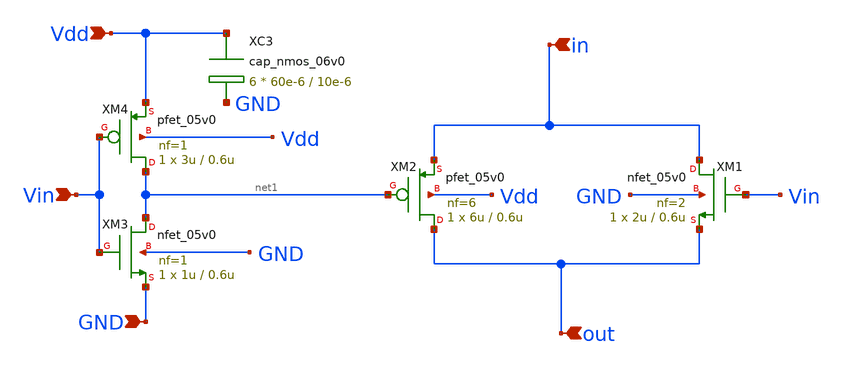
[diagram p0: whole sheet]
** sch_path: schema_ram/MG_switch/cmos_switch.sch
**.subckt cmos_switch Vdd Vin in out GND
*.ipin Vdd
*.ipin Vin
*.ipin in
*.ipin out
*.ipin GND
XM1 in Vin out GND nfet_05v0 L=0.6u W=2u nf=2 ad='int((nf+1)/2) * W/nf * 0.18u' as='int((nf+2)/2) * W/nf * 0.18u'
+ pd='2*int((nf+1)/2) * (W/nf + 0.18u)' ps='2*int((nf+2)/2) * (W/nf + 0.18u)' nrd='0.18u / W' nrs='0.18u / W'
+ sa=0 sb=0 sd=0 m=1
XM2 out net1 in Vdd pfet_05v0 L=0.6u W=6u nf=6 ad='int((nf+1)/2) * W/nf * 0.18u' as='int((nf+2)/2) * W/nf * 0.18u'
+ pd='2*int((nf+1)/2) * (W/nf + 0.18u)' ps='2*int((nf+2)/2) * (W/nf + 0.18u)' nrd='0.18u / W' nrs='0.18u / W'
+ sa=0 sb=0 sd=0 m=1
XM3 net1 Vin GND GND nfet_05v0 L=0.6u W=1u nf=1 ad='int((nf+1)/2) * W/nf * 0.18u' as='int((nf+2)/2) * W/nf * 0.18u'
+ pd='2*int((nf+1)/2) * (W/nf + 0.18u)' ps='2*int((nf+2)/2) * (W/nf + 0.18u)' nrd='0.18u / W' nrs='0.18u / W'
+ sa=0 sb=0 sd=0 m=1
XM4 net1 Vin Vdd Vdd pfet_05v0 L=0.6u W=3u nf=1 ad='int((nf+1)/2) * W/nf * 0.18u' as='int((nf+2)/2) * W/nf * 0.18u'
+ pd='2*int((nf+1)/2) * (W/nf + 0.18u)' ps='2*int((nf+2)/2) * (W/nf + 0.18u)' nrd='0.18u / W' nrs='0.18u / W'
+ sa=0 sb=0 sd=0 m=1
XC3 Vdd GND cap_nmos_06v0 c_width=60e-6 c_length=10e-6 m=6
**.ends
.end
